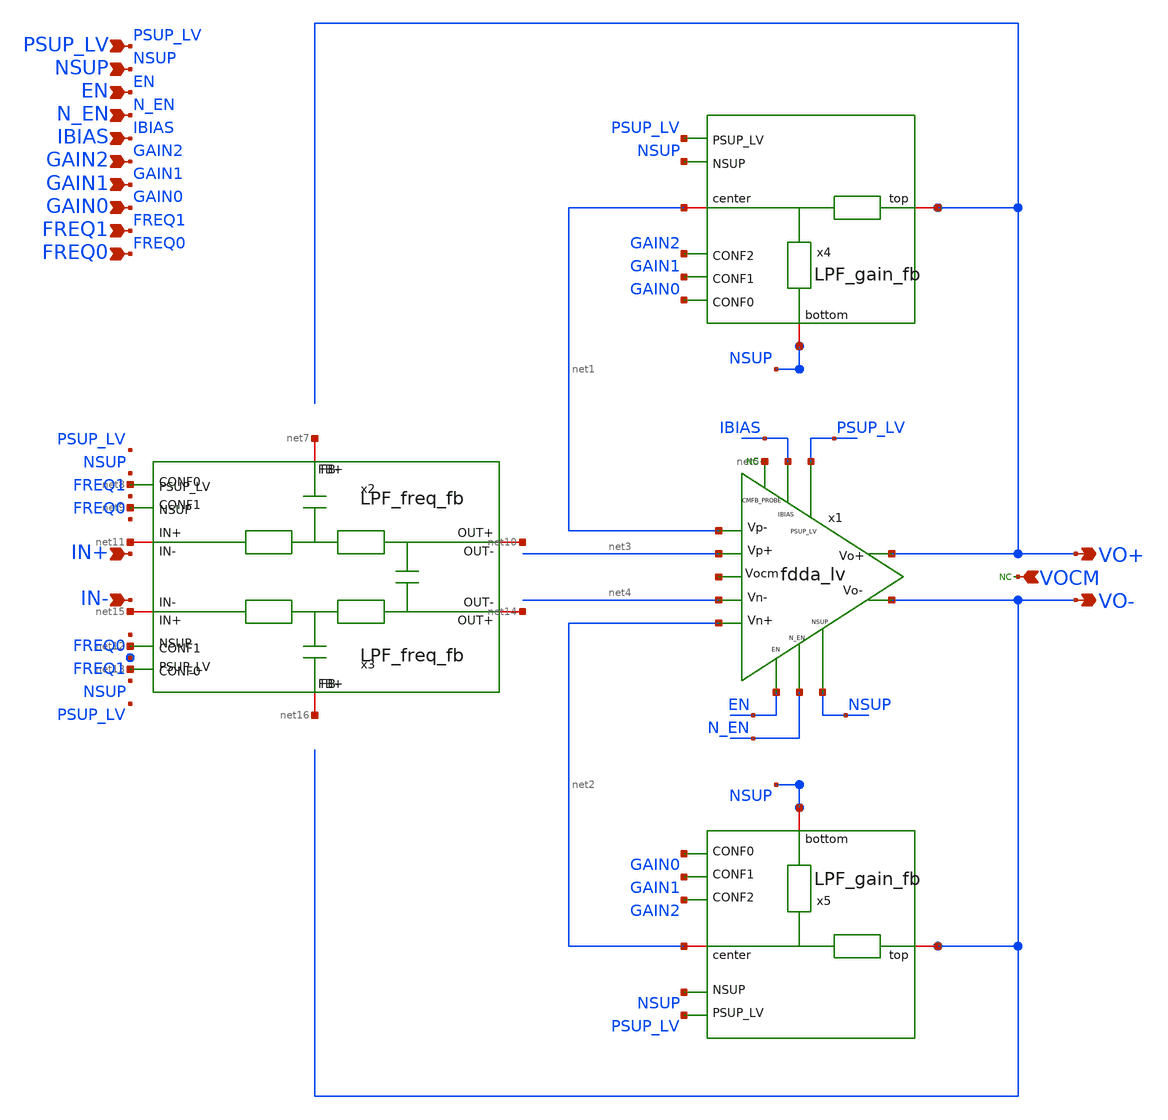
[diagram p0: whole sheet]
** sch_path: xschem/blocks/LPF/LPF.sch
**.subckt LPF NSUP EN N_EN IBIAS PSUP_LV GAIN2 VO+ VO- VOCM IN+ IN- GAIN1 GAIN0 FREQ1 FREQ0
*.ipin NSUP
*.ipin EN
*.ipin N_EN
*.ipin IBIAS
*.ipin PSUP_LV
*.ipin GAIN2
*.opin VO+
*.opin VO-
*.ipin VOCM
*.ipin IN+
*.ipin IN-
*.ipin GAIN1
*.ipin GAIN0
*.ipin FREQ1
*.ipin FREQ0
* noconn #net5
x1 PSUP_LV net1 net4 net2 net3 VO+ VO- IBIAS N_EN EN NSUP net5 net6 fdda_lv
* noconn VOCM
x2 net7 net8 net9 net10 net11 net12 net13 net14 net15 net16 LPF_freq_fb
x3 net16 net13 net12 net14 net15 net9 net8 net10 net11 net7 LPF_freq_fb
x4 VO+ net1 PSUP_LV NSUP GAIN2 GAIN1 GAIN0 NSUP LPF_gain_fb
x5 VO- net2 PSUP_LV NSUP GAIN2 GAIN1 GAIN0 NSUP LPF_gain_fb
**.ends
.end
